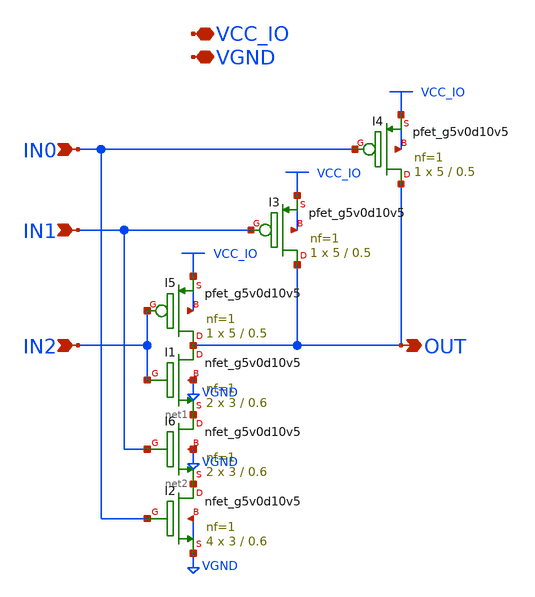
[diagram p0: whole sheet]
** sch_path: com_cclat_hvnand3.sch
* Copyright 2023 David Mitchell Bailey
* Licensed under the Apache License, Version 2.0 (the "License");
* you may not use this file except in compliance with the License.
* You may obtain a copy of the License at
* https://www.apache.org/licenses/LICENSE-2.0
* Unless required by applicable law or agreed to in writing, software
* distributed under the License is distributed on an "AS IS" BASIS,
* WITHOUT WARRANTIES OR CONDITIONS OF ANY KIND, either express or implied.
* See the License for the specific language governing permissions and
* limitations under the License.
**.subckt com_cclat_hvnand3 IN2 OUT VCC_IO VGND IN1 IN0
*.ipin IN2
*.opin OUT
*.iopin VCC_IO
*.iopin VGND
*.ipin IN1
*.ipin IN0
XI1 OUT IN2 net1 VGND sky130_fd_pr__nfet_g5v0d10v5 L=0.6 W=3 nf=1 ad='int((nf+1)/2) * W/nf * 0.29' as='int((nf+2)/2) * W/nf * 0.29'
+ pd='2*int((nf+1)/2) * (W/nf + 0.29)' ps='2*int((nf+2)/2) * (W/nf + 0.29)' nrd='0.29 / W' nrs='0.29 / W'
+ sa=0 sb=0 sd=0 mult=2 m=2
XI5 OUT IN2 VCC_IO VCC_IO sky130_fd_pr__pfet_g5v0d10v5 L=0.5 W=5 nf=1 ad='int((nf+1)/2) * W/nf * 0.29'
+ as='int((nf+2)/2) * W/nf * 0.29' pd='2*int((nf+1)/2) * (W/nf + 0.29)' ps='2*int((nf+2)/2) * (W/nf + 0.29)'
+ nrd='0.29 / W' nrs='0.29 / W' sa=0 sb=0 sd=0 mult=1 m=1
XI3 OUT IN1 VCC_IO VCC_IO sky130_fd_pr__pfet_g5v0d10v5 L=0.5 W=5 nf=1 ad='int((nf+1)/2) * W/nf * 0.29'
+ as='int((nf+2)/2) * W/nf * 0.29' pd='2*int((nf+1)/2) * (W/nf + 0.29)' ps='2*int((nf+2)/2) * (W/nf + 0.29)'
+ nrd='0.29 / W' nrs='0.29 / W' sa=0 sb=0 sd=0 mult=1 m=1
XI6 net1 IN1 net2 VGND sky130_fd_pr__nfet_g5v0d10v5 L=0.6 W=3 nf=1 ad='int((nf+1)/2) * W/nf * 0.29' as='int((nf+2)/2) * W/nf * 0.29'
+ pd='2*int((nf+1)/2) * (W/nf + 0.29)' ps='2*int((nf+2)/2) * (W/nf + 0.29)' nrd='0.29 / W' nrs='0.29 / W'
+ sa=0 sb=0 sd=0 mult=2 m=2
XI2 net2 IN0 VGND VGND sky130_fd_pr__nfet_g5v0d10v5 L=0.6 W=3 nf=1 ad='int((nf+1)/2) * W/nf * 0.29' as='int((nf+2)/2) * W/nf * 0.29'
+ pd='2*int((nf+1)/2) * (W/nf + 0.29)' ps='2*int((nf+2)/2) * (W/nf + 0.29)' nrd='0.29 / W' nrs='0.29 / W'
+ sa=0 sb=0 sd=0 mult=4 m=4
XI4 OUT IN0 VCC_IO VCC_IO sky130_fd_pr__pfet_g5v0d10v5 L=0.5 W=5 nf=1 ad='int((nf+1)/2) * W/nf * 0.29'
+ as='int((nf+2)/2) * W/nf * 0.29' pd='2*int((nf+1)/2) * (W/nf + 0.29)' ps='2*int((nf+2)/2) * (W/nf + 0.29)'
+ nrd='0.29 / W' nrs='0.29 / W' sa=0 sb=0 sd=0 mult=1 m=1
**.ends
.end
